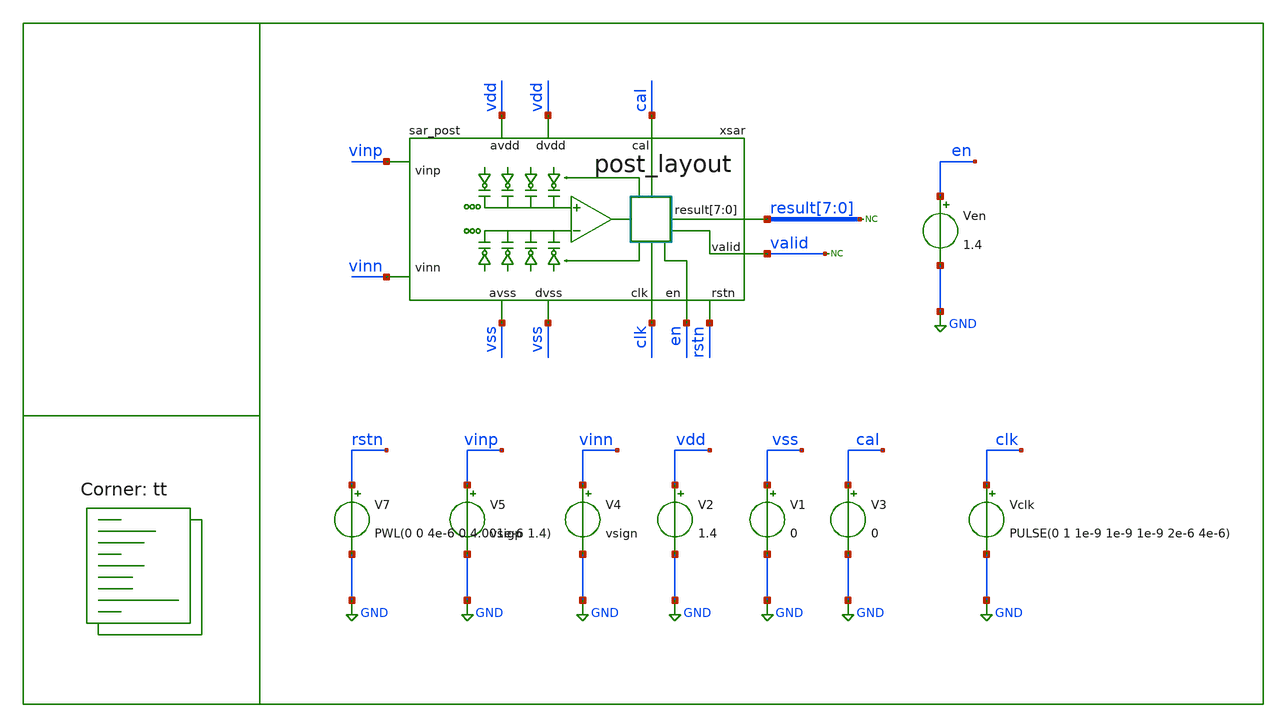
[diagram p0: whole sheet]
** sch_path: new_layout/simulations/tb_sar_new_layout.sch

.include /home/alex/Desktop/EDA/SAR_IPN/new_layout/simulations/spice/comparator.spice
.include /home/alex/Desktop/EDA/SAR_IPN/new_layout/simulations/spice/latch.spice
.include /home/alex/Desktop/EDA/SAR_IPN/new_layout/simulations/spice/dac.spice

.include /home/alex/Desktop/EDA/SAR_IPN/new_layout/simulations/spice/cmos_cells_digital.sp
.include /home/alex/Desktop/EDA/SAR_IPN/new_layout/simulations/spice/sar_logic.sp
.include $::SKYWATER_STDCELLS/sky130_fd_sc_hd.spice


.lib $::SKYWATER_MODELS/sky130.lib.spice tt
**.subckt tb_sar_new_layout
V1 vss GND 0
V2 vdd GND 1.4
V4 vinn GND vsign
V5 vinp GND vsigp
Vclk clk GND PULSE(0 1 1e-9 1e-9 1e-9 2e-6 4e-6)
Ven en GND 1.4
* noconn valid
V3 cal GND 0
* noconn result[7:0]
xsar vdd vdd vss result[7] result[6] result[5] result[4] result[3] result[2] result[1] result[0]
+ vinn vss clk vinp en valid cal rstn sar_post
V7 rstn GND PWL(0 0 4e-6 0 4.001e-6 1.4)
**.ends

* expanding   symbol:  /media/psf/Home/EDA/SAR_IPN/new_layout/simulations/symbols/sar_post.sym # of
*+ pins=12
** sym_path: post_layout/sar_post.sym
** sch_path: post_layout/sar_post.sch
.subckt sar_post avdd dvdd dvss result[7] result[6] result[5] result[4] result[3] result[2]
+ result[1] result[0] vinn avss clk vinp en valid cal rstn
*.iopin avss
*.iopin avdd
*.iopin dvss
*.iopin dvdd
*.ipin vinp
*.ipin vinn
*.opin result[7],result[6],result[5],result[4],result[3],result[2],result[1],result[0]
*.ipin clk
*.ipin en
*.opin valid
*.ipin cal
*.ipin rstn
**** begin user architecture code


Xuut dcomp dctln1 dctln0 dctlp1 dctlp0 dctln7 dctln6 dctln5 dctln4 dctln3 dctln2 dtrim4  dtrim1
+ dtrim0 dtrim2 dtrim3 dtrimb3 dtrimb2 dtrimb0 dtrimb1 dtrimb4 dctlp2 dctlp3 dctlp4 dctlp5  dctlp6 dctlp7
+ dclkc dres7 dres6 dres5 dres4 drstn dres3 dres2 dres1 dres0  dvalid dcal den dclk vinp vinn dvdd avdd
+ dvss SAR

.model adc_buff adc_bridge(in_low = 0.2 in_high=0.8)
.model dac_buff dac_bridge(out_high = 1.2)

Aad [clk rstn en comp cal] [dclk drstn den dcomp dcal] adc_buff
Ada [dctlp0 dctlp1 dctlp2 dctlp3 dctlp4 dctlp5 dctlp6 dctlp7 dctln0 dctln1 dctln2 dctln3 dctln4
+ dctln5 dctln6 dctln7 dres0 dres1 dres2 dres3 dres4 dres5 dres6 dres7 dsamp dclkc] [ctlp_0_ ctlp_1_ ctlp_2_
+ ctlp_3_ ctlp_4_ ctlp_5_ ctlp_6_ ctlp_7_ ctln_0_ ctln_1_ ctln_2_ ctln_3_ ctln_4_ ctln_5_ ctln_6_ ctln_7_
+ result_0_ result_1_ result_2_ result_3_ result_4_ result_5_ result_6_ result_7_ sample clkc] dac_buff
Ada2 [dtrim4 dtrim3 dtrim2 dtrim1 dtrim0 dtrimb4 dtrimb3 dtrimb2 dtrimb1 dtrimb0] [trim_4_ trim_3_
+ trim_2_ trim_1_ trim_0_ trimb_4_ trimb_3_ trimb_2_ trimb_1_ trimb_0_ ] dac_buff



**** end user architecture code
* noconn result[7:0]
* noconn valid
.ends

.GLOBAL GND
**** begin user architecture code

.options method trap
*.options method gear
.options gmin 1e-15
.options abstol 1e-15
.options reltol 0.0001
.options vntol 0.1e-6
.options warn 1

.param MC_SWITCH=0
.param vin=0.2
.param vcm=0.7
.param vsigp={vcm + vin/2}
.param vsign={vcm - vin/2}

.tran 100e-9 48e-6
.save all
.control

run
write tb_sar_new_layout.raw
meas tran d0 find v(xsar.res0) at=47e-6
meas tran d1 find v(xsar.res1) at=47e-6
meas tran d2 find v(xsar.res2) at=47e-6
meas tran d3 find v(xsar.res3) at=47e-6
meas tran d4 find v(xsar.res4) at=47e-6
meas tran d5 find v(xsar.res5) at=47e-6
meas tran d6 find v(xsar.res6) at=47e-6
meas tran d7 find v(xsar.res7) at=47e-6

* meas tran d0 find v(xsar.result0) at=47e-6
* meas tran d1 find v(xsar.result1) at=47e-6
* meas tran d2 find v(xsar.result2) at=47e-6
* meas tran d3 find v(xsar.result3) at=47e-6
* meas tran d4 find v(xsar.result4) at=47e-6
* meas tran d5 find v(xsar.result5) at=47e-6
* meas tran d6 find v(xsar.result6) at=47e-6
* meas tran d7 find v(xsar.result7) at=47e-6

meas tran vpmax max xsar.vp
meas tran vpmin min xsar.vp
meas tran vpend find v(xsar.vp) at=39e-6

meas tran vnmax max xsar.vn
meas tran vnmin min xsar.vn
meas tran vnend find v(xsar.vn) at=39e-6

print d0
print d1
print d2
print d3
print d4
print d5
print d6
print d7

print vpmax
print vpmin

print vnmax
print vnmin

print vpend
print vnend

.endc


**** end user architecture code
.end
